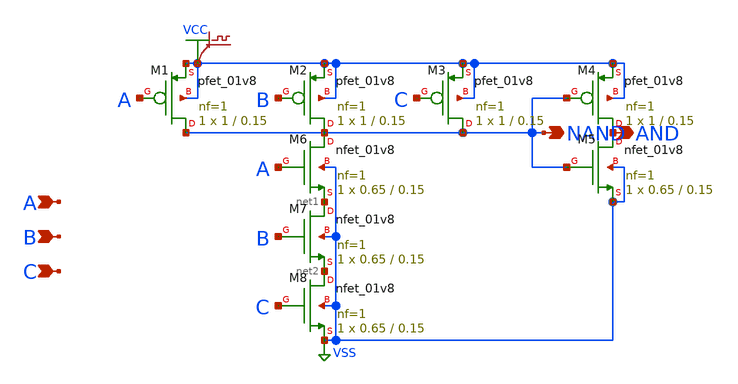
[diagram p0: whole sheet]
** sch_path: elements/nand_p3.sch
**.subckt nand_p3 A NAND AND B C
*.ipin A
*.opin NAND
*.opin AND
*.ipin B
*.ipin C
XM1 NAND A VCC VCC sky130_fd_pr__pfet_01v8 L=0.15 W=1 nf=1 ad='int((nf+1)/2) * W/nf * 0.29' as='int((nf+2)/2) * W/nf * 0.29'
+ pd='2*int((nf+1)/2) * (W/nf + 0.29)' ps='2*int((nf+2)/2) * (W/nf + 0.29)' nrd='0.29 / W' nrs='0.29 / W'
+ sa=0 sb=0 sd=0 mult=1 m=1
XM2 NAND B VCC VCC sky130_fd_pr__pfet_01v8 L=0.15 W=1 nf=1 ad='int((nf+1)/2) * W/nf * 0.29' as='int((nf+2)/2) * W/nf * 0.29'
+ pd='2*int((nf+1)/2) * (W/nf + 0.29)' ps='2*int((nf+2)/2) * (W/nf + 0.29)' nrd='0.29 / W' nrs='0.29 / W'
+ sa=0 sb=0 sd=0 mult=1 m=1
.save v(vcc)
XM3 NAND C VCC VCC sky130_fd_pr__pfet_01v8 L=0.15 W=1 nf=1 ad='int((nf+1)/2) * W/nf * 0.29' as='int((nf+2)/2) * W/nf * 0.29'
+ pd='2*int((nf+1)/2) * (W/nf + 0.29)' ps='2*int((nf+2)/2) * (W/nf + 0.29)' nrd='0.29 / W' nrs='0.29 / W'
+ sa=0 sb=0 sd=0 mult=1 m=1
XM6 NAND A net1 VSS sky130_fd_pr__nfet_01v8 L=0.15 W=0.65 nf=1 ad='int((1 + 1)/2) * 0.65 / 1 * 0.29'
+ as='int((1 + 2)/2) * 0.65 / 1 * 0.29' pd='2*int((1 + 1)/2) * (0.65 / 1 + 0.29)' ps='2*int((1 + 2)/2) * (0.65 / 1 + 0.29)'
+ nrd='0.29 / 0.65 ' nrs='0.29 / 0.65 ' sa=0 sb=0 sd=0 mult=1 m=1
XM7 net1 B net2 VSS sky130_fd_pr__nfet_01v8 L=0.15 W=0.65 nf=1 ad='int((1 + 1)/2) * 0.65 / 1 * 0.29'
+ as='int((1 + 2)/2) * 0.65 / 1 * 0.29' pd='2*int((1 + 1)/2) * (0.65 / 1 + 0.29)' ps='2*int((1 + 2)/2) * (0.65 / 1 + 0.29)'
+ nrd='0.29 / 0.65 ' nrs='0.29 / 0.65 ' sa=0 sb=0 sd=0 mult=1 m=1
XM8 net2 C VSS VSS sky130_fd_pr__nfet_01v8 L=0.15 W=0.65 nf=1 ad='int((1 + 1)/2) * 0.65 / 1 * 0.29' as='int((1 + 2)/2) * 0.65 / 1 * 0.29'
+ pd='2*int((1 + 1)/2) * (0.65 / 1 + 0.29)' ps='2*int((1 + 2)/2) * (0.65 / 1 + 0.29)' nrd='0.29 / 0.65 '
+ nrs='0.29 / 0.65 ' sa=0 sb=0 sd=0 mult=1 m=1
XM4 AND NAND VCC VCC sky130_fd_pr__pfet_01v8 L=0.15 W=1 nf=1 ad='int((nf+1)/2) * W/nf * 0.29' as='int((nf+2)/2) * W/nf * 0.29'
+ pd='2*int((nf+1)/2) * (W/nf + 0.29)' ps='2*int((nf+2)/2) * (W/nf + 0.29)' nrd='0.29 / W' nrs='0.29 / W'
+ sa=0 sb=0 sd=0 mult=1 m=1
XM5 AND NAND VSS VSS sky130_fd_pr__nfet_01v8 L=0.15 W=0.65 nf=1 ad='int((1 + 1)/2) * 0.65 / 1 * 0.29'
+ as='int((1 + 2)/2) * 0.65 / 1 * 0.29' pd='2*int((1 + 1)/2) * (0.65 / 1 + 0.29)' ps='2*int((1 + 2)/2) * (0.65 / 1 + 0.29)'
+ nrd='0.29 / 0.65 ' nrs='0.29 / 0.65 ' sa=0 sb=0 sd=0 mult=1 m=1
**.ends
.GLOBAL VCC
.GLOBAL VSS
.end
